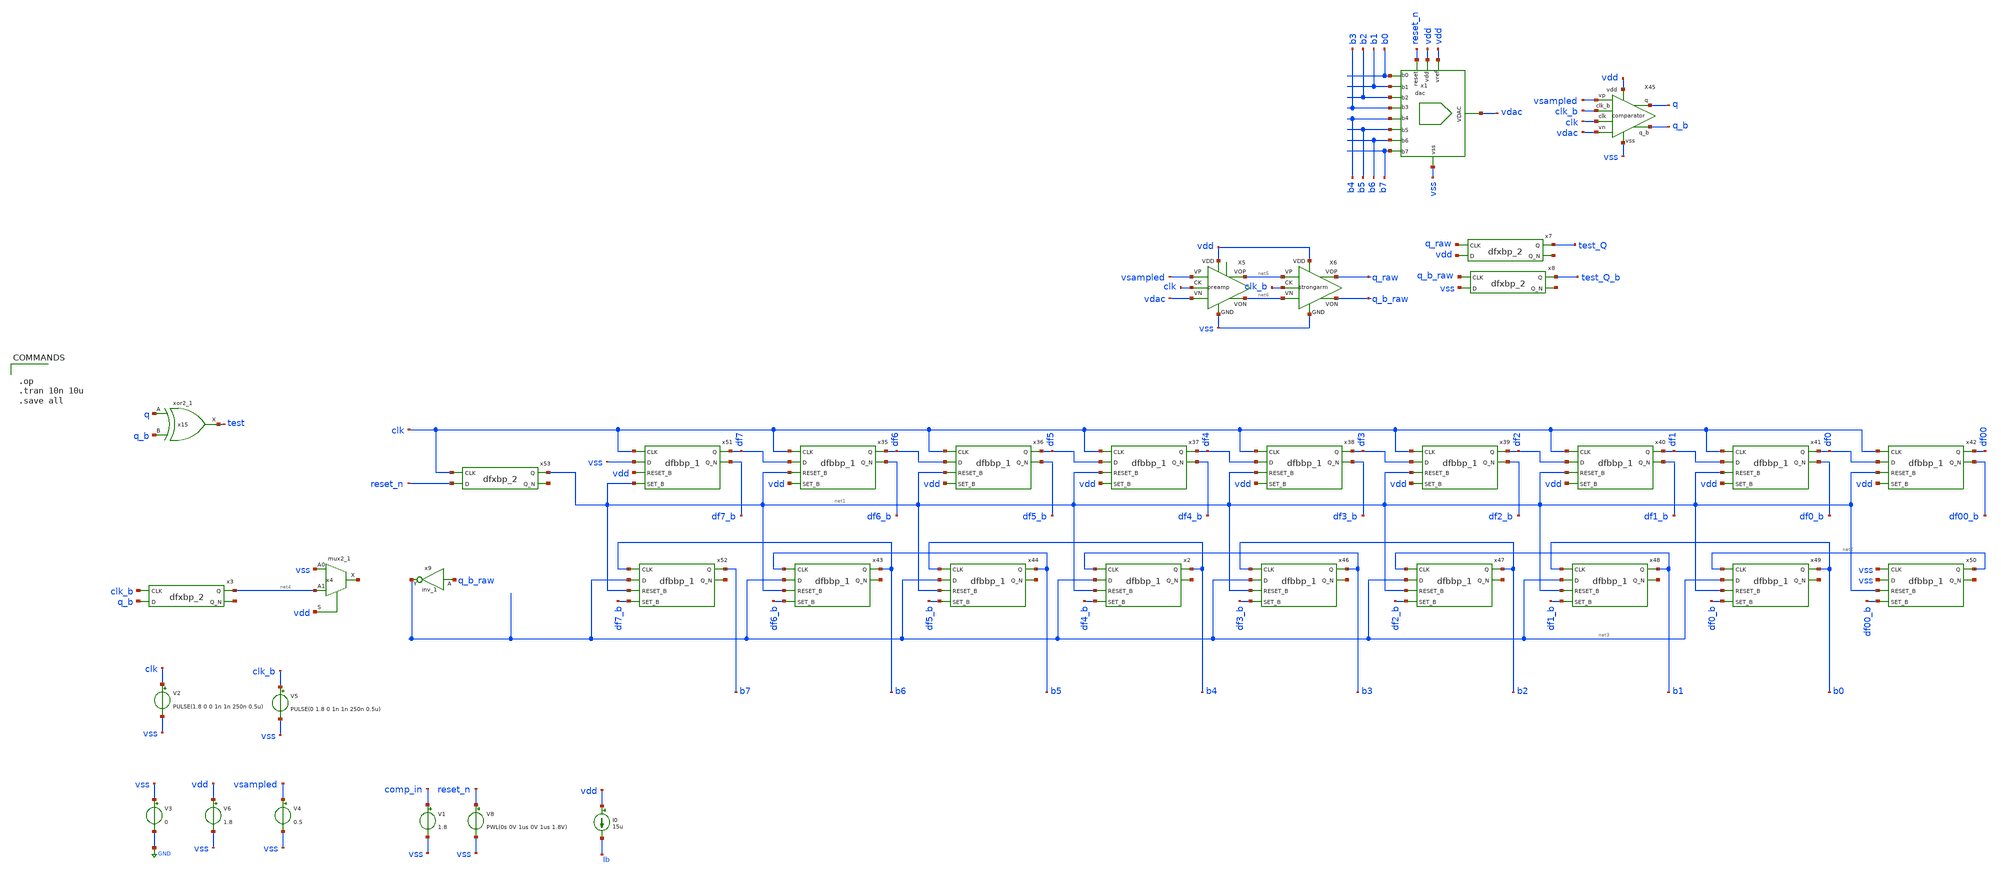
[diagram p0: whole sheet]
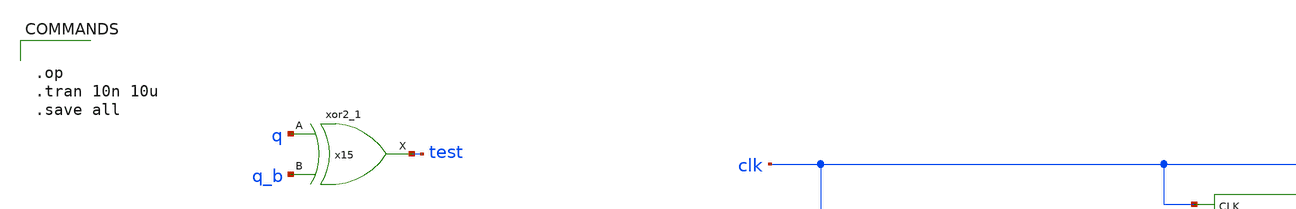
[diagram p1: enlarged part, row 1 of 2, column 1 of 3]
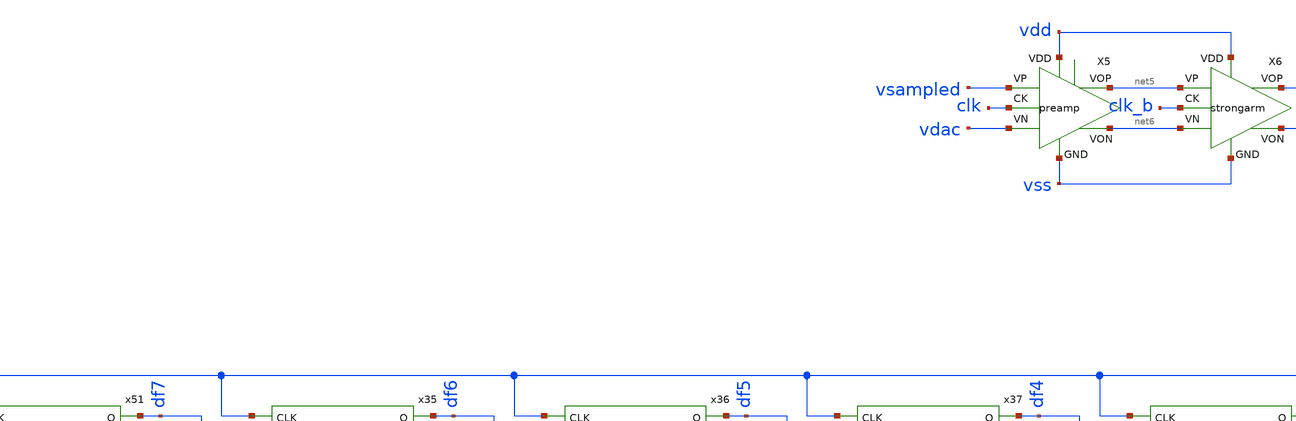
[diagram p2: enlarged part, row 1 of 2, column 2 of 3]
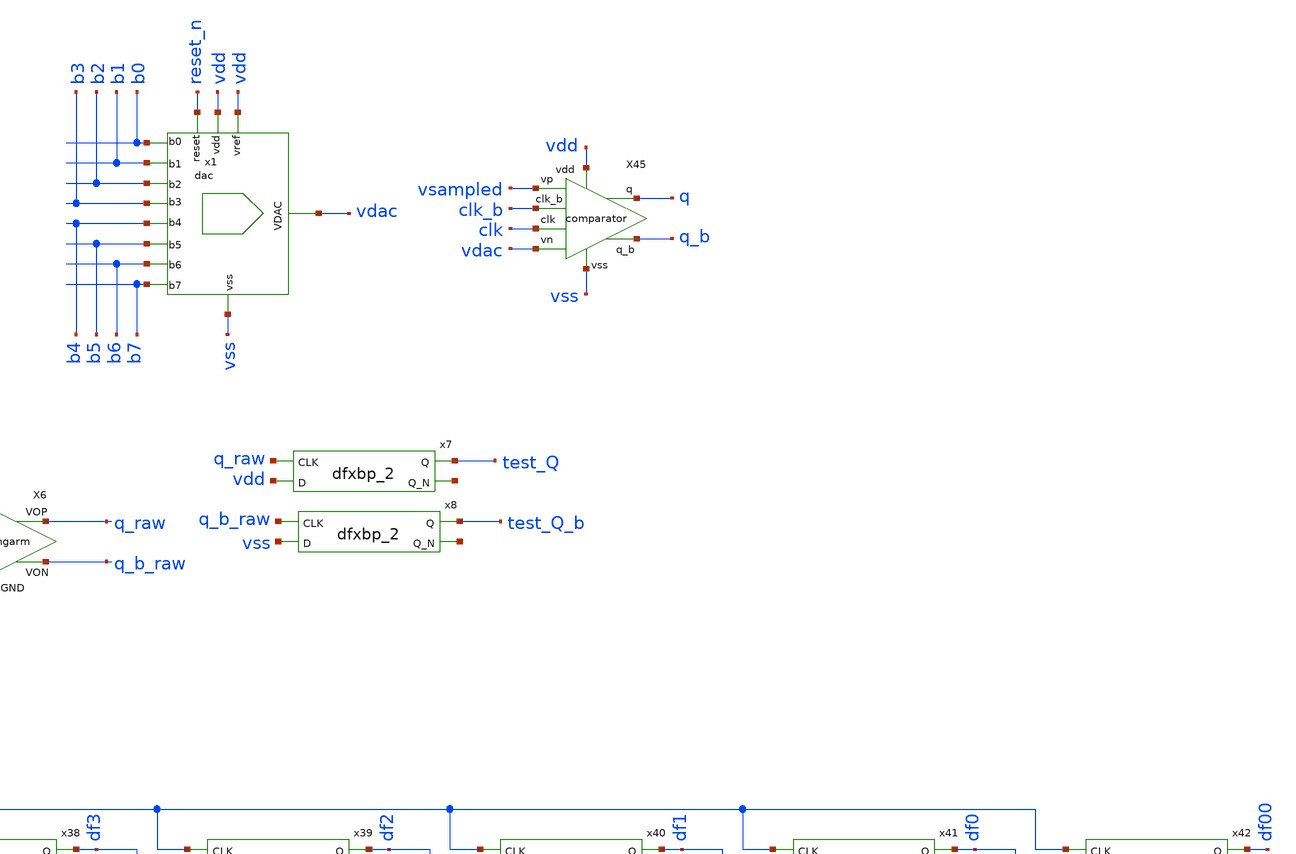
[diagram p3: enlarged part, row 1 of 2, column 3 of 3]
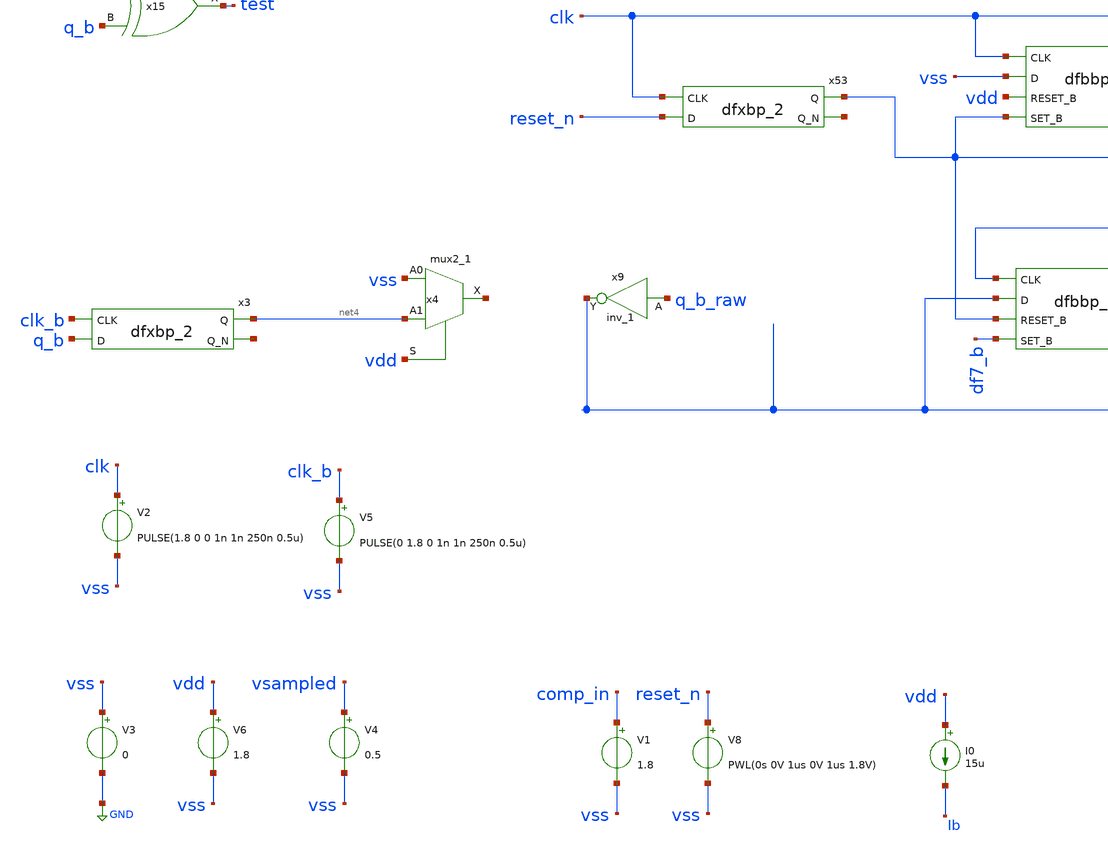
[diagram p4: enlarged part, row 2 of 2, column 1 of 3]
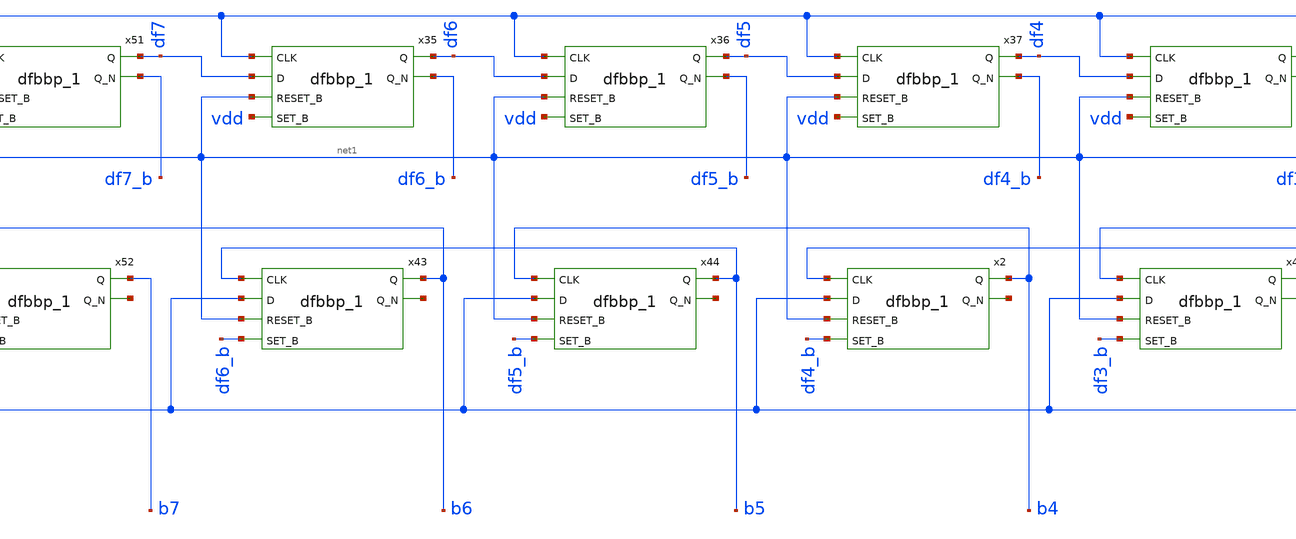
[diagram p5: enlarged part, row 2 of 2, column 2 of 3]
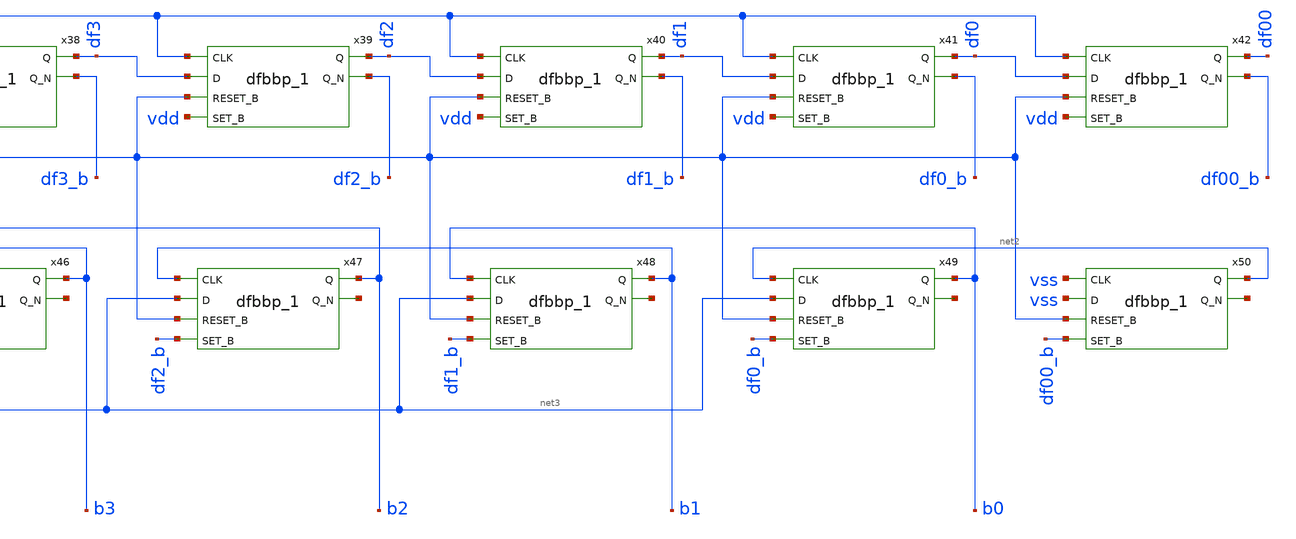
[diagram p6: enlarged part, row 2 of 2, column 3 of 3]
** sch_path: xschem/sar_logic/sar_logic_tb.sch
.lib $::SKYWATER_MODELS/sky130.lib.spice tt
.include $::SKYWATER_STDCELLS/sky130_fd_sc_hd.spice

**.subckt sar_logic_tb
V2 clk vss PULSE(1.8 0 0 1n 1n 250n 0.5u)
V1 comp_in vss 1.8
V6 vdd vss 1.8
V8 reset_n vss PWL(0s 0V 1us 0V 1us 1.8V)
I0 vdd Ib 15u
x1 vss vdac vdd vdd b0 b1 b2 b3 b4 b5 b6 b7 reset_n dac
V3 vss GND 0
V5 clk_b vss PULSE(0 1.8 0 1n 1n 250n 0.5u)
X45 vsampled vdac vss q_b q vdd clk clk_b comparator
V4 vsampled vss 0.5
x35 clk df7 net1 vdd vss vss vdd vdd df6 df6_b sky130_fd_sc_hd__dfbbp_1
x36 clk df6 net1 vdd vss vss vdd vdd df5 df5_b sky130_fd_sc_hd__dfbbp_1
x37 clk df5 net1 vdd vss vss vdd vdd df4 df4_b sky130_fd_sc_hd__dfbbp_1
x38 clk df4 net1 vdd vss vss vdd vdd df3 df3_b sky130_fd_sc_hd__dfbbp_1
x39 clk df3 net1 vdd vss vss vdd vdd df2 df2_b sky130_fd_sc_hd__dfbbp_1
x40 clk df2 net1 vdd vss vss vdd vdd df1 df1_b sky130_fd_sc_hd__dfbbp_1
x41 clk df1 net1 vdd vss vss vdd vdd df0 df0_b sky130_fd_sc_hd__dfbbp_1
x42 clk df0 net1 vdd vss vss vdd vdd df00 df00_b sky130_fd_sc_hd__dfbbp_1
x43 b5 net3 net1 df6_b vss vss vdd vdd b6 net7 sky130_fd_sc_hd__dfbbp_1
x44 b4 net3 net1 df5_b vss vss vdd vdd b5 net8 sky130_fd_sc_hd__dfbbp_1
x2 b3 net3 net1 df4_b vss vss vdd vdd b4 net9 sky130_fd_sc_hd__dfbbp_1
x46 b2 net3 net1 df3_b vss vss vdd vdd b3 net10 sky130_fd_sc_hd__dfbbp_1
x47 b1 net3 net1 df2_b vss vss vdd vdd b2 net11 sky130_fd_sc_hd__dfbbp_1
x48 b0 net3 net1 df1_b vss vss vdd vdd b1 net12 sky130_fd_sc_hd__dfbbp_1
x49 net2 net3 net1 df0_b vss vss vdd vdd b0 net13 sky130_fd_sc_hd__dfbbp_1
x50 vss vss net1 df00_b vss vss vdd vdd net2 net14 sky130_fd_sc_hd__dfbbp_1
x51 clk vss vdd net1 vss vss vdd vdd df7 df7_b sky130_fd_sc_hd__dfbbp_1
x52 b6 net3 net1 df7_b vss vss vdd vdd b7 net15 sky130_fd_sc_hd__dfbbp_1
x53 clk reset_n vss vss vdd vdd net1 net16 sky130_fd_sc_hd__dfxbp_2
x3 clk_b q_b vss vss vdd vdd net4 net17 sky130_fd_sc_hd__dfxbp_2
x4 vss net4 vdd vss vss vdd vdd net18 sky130_fd_sc_hd__mux2_1
x15 q q_b vss vss vdd vdd test sky130_fd_sc_hd__xor2_1
X5 vsampled vdac vss net6 net5 vdd clk preamp
X6 net5 net6 vss q_b_raw q_raw vdd clk_b strongarm
x7 q_raw vdd vss vss vdd vdd test_Q net19 sky130_fd_sc_hd__dfxbp_2
x8 q_b_raw vss vss vss vdd vdd test_Q_b net20 sky130_fd_sc_hd__dfxbp_2
x9 q_b_raw vss vss vdd vdd net3 sky130_fd_sc_hd__inv_1
**** begin user architecture code


.op
.tran 10n 10u
.save all


**** end user architecture code
**.ends

* expanding   symbol:  xschem/dac/dac.sym # of pins=13
** sym_path: xschem/dac/dac.sym
** sch_path: xschem/dac/dac.sch
.subckt dac vss vdac vdd vref s0 s1 s2 s3 s4 s5 s6 s7 reset
*.ipin s7
*.ipin s6
*.ipin s5
*.ipin s4
*.ipin s3
*.ipin s2
*.ipin s1
*.ipin s0
*.iopin vdd
*.iopin vss
*.iopin vref
*.opin vdac
*.ipin reset
XC2 net1 net2 sky130_fd_pr__cap_mim_m3_1 W=w L=l MF=8 m=8
X2 net2 vref vss vdd net14 vss dac_sw
XC1 net1 net3 sky130_fd_pr__cap_mim_m3_1 W=w L=l MF=4 m=4
X3 net3 vref vss vdd net15 vss dac_sw
X4 net4 vref vss vdd net16 vss dac_sw
X5 net5 vref vss vdd net17 vss dac_sw
XC3 net1 net4 sky130_fd_pr__cap_mim_m3_1 W=w L=l MF=2 m=2
XC4 net1 net5 sky130_fd_pr__cap_mim_m3_1 W=w L=l MF=1 m=1
XC5 vss net1 sky130_fd_pr__cap_mim_m3_1 W=w L=l MF=1 m=1
X1 net6 vref vss vdd net13 vss dac_sw
X6 net7 vref vss vdd net12 vss dac_sw
X7 net8 vref vss vdd net11 vss dac_sw
X8 net9 vref vss vdd net10 vss dac_sw
x9 vss s7 reset vss vss vdd vdd net10 sky130_fd_sc_hd__mux2_1
x10 vss s6 reset vss vss vdd vdd net11 sky130_fd_sc_hd__mux2_1
x11 vss s5 reset vss vss vdd vdd net12 sky130_fd_sc_hd__mux2_1
x12 vss s4 reset vss vss vdd vdd net13 sky130_fd_sc_hd__mux2_1
x13 vss s3 reset vss vss vdd vdd net14 sky130_fd_sc_hd__mux2_1
x14 vss s2 reset vss vss vdd vdd net15 sky130_fd_sc_hd__mux2_1
x15 vss s1 reset vss vss vdd vdd net16 sky130_fd_sc_hd__mux2_1
x16 vss s0 reset vss vss vdd vdd net17 sky130_fd_sc_hd__mux2_1
XM1 vdac net18 vss vss sky130_fd_pr__nfet_01v8 L=0.15 W=5 nf=1 ad='int((nf+1)/2) * W/nf * 0.29' as='int((nf+2)/2) * W/nf * 0.29'
+ pd='2*int((nf+1)/2) * (W/nf + 0.29)' ps='2*int((nf+2)/2) * (W/nf + 0.29)' nrd='0.29 / W' nrs='0.29 / W'
+ sa=0 sb=0 sd=0 mult=1 m=1
x17 reset vss vss vdd vdd net18 sky130_fd_sc_hd__inv_1
XC10 net1 vdac sky130_fd_pr__cap_mim_m3_1 W=w L=l MF=8/7 m=8/7
XC6 vdac net9 sky130_fd_pr__cap_mim_m3_1 W=w L=l MF=8 m=8
XC7 vdac net8 sky130_fd_pr__cap_mim_m3_1 W=w L=l MF=4 m=4
XC8 vdac net7 sky130_fd_pr__cap_mim_m3_1 W=w L=l MF=2 m=2
XC9 vdac net6 sky130_fd_pr__cap_mim_m3_1 W=w L=l MF=1 m=1
.ends


* expanding   symbol:  xschem/comparator/comparator.sym # of pins=8
** sym_path: xschem/comparator/comparator.sym
** sch_path: xschem/comparator/comparator.sch
.subckt comparator vp vn vss q_b q vdd clk clk_b
*.ipin vp
*.ipin vn
*.iopin vdd
*.ipin clk
*.iopin vss
*.opin q
*.opin q_b
*.ipin clk_b
X6 net3 net4 vss net2 net1 vdd clk_b strongarm
XM5 q_b q_comp vss vss sky130_fd_pr__nfet_01v8 L=0.15 W=0.5 nf=1 ad='int((1 + 1)/2) * 0.5 / 1 * 0.29'
+ as='int((1 + 2)/2) * 0.5 / 1 * 0.29' pd='2*int((1 + 1)/2) * (0.5 / 1 + 0.29)' ps='2*int((1 + 2)/2) * (0.5 / 1 + 0.29)'
+ nrd='0.29 / 0.5 ' nrs='0.29 / 0.5 ' sa=0 sb=0 sd=0 mult=1 m=1
XM1 q q_b_comp vss vss sky130_fd_pr__nfet_01v8 L=0.15 W=0.5 nf=1 ad='int((1 + 1)/2) * 0.5 / 1 * 0.29'
+ as='int((1 + 2)/2) * 0.5 / 1 * 0.29' pd='2*int((1 + 1)/2) * (0.5 / 1 + 0.29)' ps='2*int((1 + 2)/2) * (0.5 / 1 + 0.29)'
+ nrd='0.29 / 0.5 ' nrs='0.29 / 0.5 ' sa=0 sb=0 sd=0 mult=1 m=1
x5 q_b vss vss vdd vdd q sky130_fd_sc_hd__inv_1
x7 q vss vss vdd vdd q_b sky130_fd_sc_hd__inv_1
x1 net1 vss vss vdd vdd q_comp sky130_fd_sc_hd__inv_1
x2 net2 vss vss vdd vdd q_b_comp sky130_fd_sc_hd__inv_1
X3 clk vn vp net3 vdd vss net4 ota_5t
.ends


* expanding   symbol:  xschem/comparator/preamp.sym # of pins=7
** sym_path: xschem/comparator/preamp.sym
** sch_path: xschem/comparator/preamp.sch
.subckt preamp VP VN GND VON VOP VDD CK
*.iopin VDD
*.iopin GND
*.iopin CK
*.iopin VON
*.iopin VOP
*.iopin VP
*.iopin VN
XM5 VON VP net1 GND sky130_fd_pr__nfet_01v8 L=1.5 W=2 nf=2 ad='int((2 + 1)/2) * 2 / 2 * 0.29' as='int((2 + 2)/2) * 2 / 2 * 0.29'
+ pd='2*int((2 + 1)/2) * (2 / 2 + 0.29)' ps='2*int((2 + 2)/2) * (2 / 2 + 0.29)' nrd='0.29 / 2 ' nrs='0.29 / 2 '
+ sa=0 sb=0 sd=0 mult=1 m=1
XM6 VON VON VDD VDD sky130_fd_pr__pfet_01v8 L=1.5 W=4 nf=1 ad='int((nf+1)/2) * W/nf * 0.29' as='int((nf+2)/2) * W/nf * 0.29'
+ pd='2*int((nf+1)/2) * (W/nf + 0.29)' ps='2*int((nf+2)/2) * (W/nf + 0.29)' nrd='0.29 / W' nrs='0.29 / W'
+ sa=0 sb=0 sd=0 mult=1 m=1
XM7 VOP VOP VDD VDD sky130_fd_pr__pfet_01v8 L=1.5 W=4 nf=1 ad='int((nf+1)/2) * W/nf * 0.29' as='int((nf+2)/2) * W/nf * 0.29'
+ pd='2*int((nf+1)/2) * (W/nf + 0.29)' ps='2*int((nf+2)/2) * (W/nf + 0.29)' nrd='0.29 / W' nrs='0.29 / W'
+ sa=0 sb=0 sd=0 mult=1 m=1
XM8 VOP VN net1 GND sky130_fd_pr__nfet_01v8 L=1.5 W=2 nf=2 ad='int((2 + 1)/2) * 2 / 2 * 0.29' as='int((2 + 2)/2) * 2 / 2 * 0.29'
+ pd='2*int((2 + 1)/2) * (2 / 2 + 0.29)' ps='2*int((2 + 2)/2) * (2 / 2 + 0.29)' nrd='0.29 / 2 ' nrs='0.29 / 2 '
+ sa=0 sb=0 sd=0 mult=1 m=1
XM9 net1 CK GND GND sky130_fd_pr__nfet_01v8 L=1 W=4 nf=1 ad='int((1 + 1)/2) * 4 / 1 * 0.29' as='int((1 + 2)/2) * 4 / 1 * 0.29'
+ pd='2*int((1 + 1)/2) * (4 / 1 + 0.29)' ps='2*int((1 + 2)/2) * (4 / 1 + 0.29)' nrd='0.29 / 4 ' nrs='0.29 / 4 '
+ sa=0 sb=0 sd=0 mult=1 m=1
.ends


* expanding   symbol:  xschem/comparator/strongarm.sym # of pins=7
** sym_path: xschem/comparator/strongarm.sym
** sch_path: xschem/comparator/strongarm.sch
.subckt strongarm VP VN GND VON VOP VDD CK
*.iopin GND
*.ipin VP
*.opin VOP
*.opin VON
*.ipin VN
*.iopin VDD
*.ipin CK
XM2 net2 CK GND GND sky130_fd_pr__nfet_01v8 L=0.15 W=2 nf=2 ad='int((nf+1)/2) * W/nf * 0.29' as='int((nf+2)/2) * W/nf * 0.29'
+ pd='2*int((nf+1)/2) * (W/nf + 0.29)' ps='2*int((nf+2)/2) * (W/nf + 0.29)' nrd='0.29 / W' nrs='0.29 / W'
+ sa=0 sb=0 sd=0 mult=1 m=1
XM4 VON CK VDD VDD sky130_fd_pr__pfet_01v8 L=0.15 W=1 nf=1 ad='int((nf+1)/2) * W/nf * 0.29' as='int((nf+2)/2) * W/nf * 0.29'
+ pd='2*int((nf+1)/2) * (W/nf + 0.29)' ps='2*int((nf+2)/2) * (W/nf + 0.29)' nrd='0.29 / W' nrs='0.29 / W'
+ sa=0 sb=0 sd=0 mult=1 m=1
XM5 net1 CK VDD VDD sky130_fd_pr__pfet_01v8 L=0.15 W=1 nf=1 ad='int((nf+1)/2) * W/nf * 0.29' as='int((nf+2)/2) * W/nf * 0.29'
+ pd='2*int((nf+1)/2) * (W/nf + 0.29)' ps='2*int((nf+2)/2) * (W/nf + 0.29)' nrd='0.29 / W' nrs='0.29 / W'
+ sa=0 sb=0 sd=0 mult=1 m=1
XM8 net1 VP net2 GND sky130_fd_pr__nfet_01v8 L=0.15 W=2.5 nf=4 ad='int((nf+1)/2) * W/nf * 0.29' as='int((nf+2)/2) * W/nf * 0.29'
+ pd='2*int((nf+1)/2) * (W/nf + 0.29)' ps='2*int((nf+2)/2) * (W/nf + 0.29)' nrd='0.29 / W' nrs='0.29 / W'
+ sa=0 sb=0 sd=0 mult=1 m=1
XM9 VON VOP net1 GND sky130_fd_pr__nfet_01v8 L=0.15 W=2.5 nf=4 ad='int((nf+1)/2) * W/nf * 0.29' as='int((nf+2)/2) * W/nf * 0.29'
+ pd='2*int((nf+1)/2) * (W/nf + 0.29)' ps='2*int((nf+2)/2) * (W/nf + 0.29)' nrd='0.29 / W' nrs='0.29 / W'
+ sa=0 sb=0 sd=0 mult=1 m=1
XM11 VOP CK VDD VDD sky130_fd_pr__pfet_01v8 L=0.15 W=1 nf=1 ad='int((nf+1)/2) * W/nf * 0.29' as='int((nf+2)/2) * W/nf * 0.29'
+ pd='2*int((nf+1)/2) * (W/nf + 0.29)' ps='2*int((nf+2)/2) * (W/nf + 0.29)' nrd='0.29 / W' nrs='0.29 / W'
+ sa=0 sb=0 sd=0 mult=1 m=1
XM12 net3 CK VDD VDD sky130_fd_pr__pfet_01v8 L=0.15 W=1 nf=1 ad='int((nf+1)/2) * W/nf * 0.29' as='int((nf+2)/2) * W/nf * 0.29'
+ pd='2*int((nf+1)/2) * (W/nf + 0.29)' ps='2*int((nf+2)/2) * (W/nf + 0.29)' nrd='0.29 / W' nrs='0.29 / W'
+ sa=0 sb=0 sd=0 mult=1 m=1
XM13 net3 VN net2 GND sky130_fd_pr__nfet_01v8 L=0.15 W=2.5 nf=4 ad='int((nf+1)/2) * W/nf * 0.29' as='int((nf+2)/2) * W/nf * 0.29'
+ pd='2*int((nf+1)/2) * (W/nf + 0.29)' ps='2*int((nf+2)/2) * (W/nf + 0.29)' nrd='0.29 / W' nrs='0.29 / W'
+ sa=0 sb=0 sd=0 mult=1 m=1
XM14 VOP VON net3 GND sky130_fd_pr__nfet_01v8 L=0.15 W=10 nf=1 ad='int((nf+1)/2) * W/nf * 0.29' as='int((nf+2)/2) * W/nf * 0.29'
+ pd='2*int((nf+1)/2) * (W/nf + 0.29)' ps='2*int((nf+2)/2) * (W/nf + 0.29)' nrd='0.29 / W' nrs='0.29 / W'
+ sa=0 sb=0 sd=0 mult=1 m=1
XM15 VOP VON VDD VDD sky130_fd_pr__pfet_01v8 L=0.15 W=2.5 nf=1 ad='int((nf+1)/2) * W/nf * 0.29' as='int((nf+2)/2) * W/nf * 0.29'
+ pd='2*int((nf+1)/2) * (W/nf + 0.29)' ps='2*int((nf+2)/2) * (W/nf + 0.29)' nrd='0.29 / W' nrs='0.29 / W'
+ sa=0 sb=0 sd=0 mult=1 m=1
XM10 VON VOP VDD VDD sky130_fd_pr__pfet_01v8 L=0.15 W=2.5 nf=1 ad='int((nf+1)/2) * W/nf * 0.29' as='int((nf+2)/2) * W/nf * 0.29'
+ pd='2*int((nf+1)/2) * (W/nf + 0.29)' ps='2*int((nf+2)/2) * (W/nf + 0.29)' nrd='0.29 / W' nrs='0.29 / W'
+ sa=0 sb=0 sd=0 mult=1 m=1
.ends


* expanding   symbol:  xschem/dac/dac_sw.sym # of pins=6
** sym_path: xschem/dac/dac_sw.sym
** sch_path: xschem/dac/dac_sw.sch
.subckt dac_sw c b vss vdd clk a
*.iopin vdd
*.iopin vss
*.ipin clk
*.iopin c
*.iopin a
*.iopin b
XM2 c clk b vss sky130_fd_pr__nfet_01v8 L=0.15 W=10 nf=1 ad='int((nf+1)/2) * W/nf * 0.29' as='int((nf+2)/2) * W/nf * 0.29'
+ pd='2*int((nf+1)/2) * (W/nf + 0.29)' ps='2*int((nf+2)/2) * (W/nf + 0.29)' nrd='0.29 / W' nrs='0.29 / W'
+ sa=0 sb=0 sd=0 mult=1 m=1
XM5 b net1 c vdd sky130_fd_pr__pfet_01v8 L=0.15 W=20 nf=1 ad='int((nf+1)/2) * W/nf * 0.29' as='int((nf+2)/2) * W/nf * 0.29'
+ pd='2*int((nf+1)/2) * (W/nf + 0.29)' ps='2*int((nf+2)/2) * (W/nf + 0.29)' nrd='0.29 / W' nrs='0.29 / W'
+ sa=0 sb=0 sd=0 mult=1 m=1
XM6 c net1 a vss sky130_fd_pr__nfet_01v8 L=0.15 W=10 nf=1 ad='int((nf+1)/2) * W/nf * 0.29' as='int((nf+2)/2) * W/nf * 0.29'
+ pd='2*int((nf+1)/2) * (W/nf + 0.29)' ps='2*int((nf+2)/2) * (W/nf + 0.29)' nrd='0.29 / W' nrs='0.29 / W'
+ sa=0 sb=0 sd=0 mult=1 m=1
XM7 a clk c vdd sky130_fd_pr__pfet_01v8 L=0.15 W=20 nf=1 ad='int((nf+1)/2) * W/nf * 0.29' as='int((nf+2)/2) * W/nf * 0.29'
+ pd='2*int((nf+1)/2) * (W/nf + 0.29)' ps='2*int((nf+2)/2) * (W/nf + 0.29)' nrd='0.29 / W' nrs='0.29 / W'
+ sa=0 sb=0 sd=0 mult=1 m=1
x1 clk vss vss vdd vdd net1 sky130_fd_sc_hd__inv_1
.ends


* expanding   symbol:  xschem/preamp/ota_5t.sym # of pins=7
** sym_path: xschem/preamp/ota_5t.sym
** sch_path: xschem/preamp/ota_5t.sch
.subckt ota_5t VB VIN VIP VOP VDD VSS VON
*.iopin VDD
*.iopin VSS
*.opin VOP
*.ipin VIP
*.ipin VIN
*.ipin VB
*.opin VON
XM3 VON VIP net1 VSS sky130_fd_pr__nfet_01v8 L=1 W=5 nf=2 ad='int((2 + 1)/2) * 5 / 2 * 0.29' as='int((2 + 2)/2) * 5 / 2 * 0.29'
+ pd='2*int((2 + 1)/2) * (5 / 2 + 0.29)' ps='2*int((2 + 2)/2) * (5 / 2 + 0.29)' nrd='0.29 / 5 ' nrs='0.29 / 5 '
+ sa=0 sb=0 sd=0 mult=1 m=1
XM1 VOP VOP VDD VDD sky130_fd_pr__pfet_01v8 L=2.5 W=1.5 nf=2 ad='int((nf+1)/2) * W/nf * 0.29' as='int((nf+2)/2) * W/nf * 0.29'
+ pd='2*int((nf+1)/2) * (W/nf + 0.29)' ps='2*int((nf+2)/2) * (W/nf + 0.29)' nrd='0.29 / W' nrs='0.29 / W'
+ sa=0 sb=0 sd=0 mult=1 m=1
XM4 VOP VIN net1 VSS sky130_fd_pr__nfet_01v8 L=1 W=5 nf=2 ad='int((2 + 1)/2) * 5 / 2 * 0.29' as='int((2 + 2)/2) * 5 / 2 * 0.29'
+ pd='2*int((2 + 1)/2) * (5 / 2 + 0.29)' ps='2*int((2 + 2)/2) * (5 / 2 + 0.29)' nrd='0.29 / 5 ' nrs='0.29 / 5 '
+ sa=0 sb=0 sd=0 mult=1 m=1
XM5 net1 VB VSS VSS sky130_fd_pr__nfet_01v8 L=0.15 W=2 nf=1 ad='int((1 + 1)/2) * 2 / 1 * 0.29' as='int((1 + 2)/2) * 2 / 1 * 0.29'
+ pd='2*int((1 + 1)/2) * (2 / 1 + 0.29)' ps='2*int((1 + 2)/2) * (2 / 1 + 0.29)' nrd='0.29 / 2 ' nrs='0.29 / 2 '
+ sa=0 sb=0 sd=0 mult=1 m=1
XM8 VON VON VDD VDD sky130_fd_pr__pfet_01v8 L=2.5 W=1.5 nf=2 ad='int((nf+1)/2) * W/nf * 0.29' as='int((nf+2)/2) * W/nf * 0.29'
+ pd='2*int((nf+1)/2) * (W/nf + 0.29)' ps='2*int((nf+2)/2) * (W/nf + 0.29)' nrd='0.29 / W' nrs='0.29 / W'
+ sa=0 sb=0 sd=0 mult=1 m=1
.ends

.GLOBAL GND
.end
